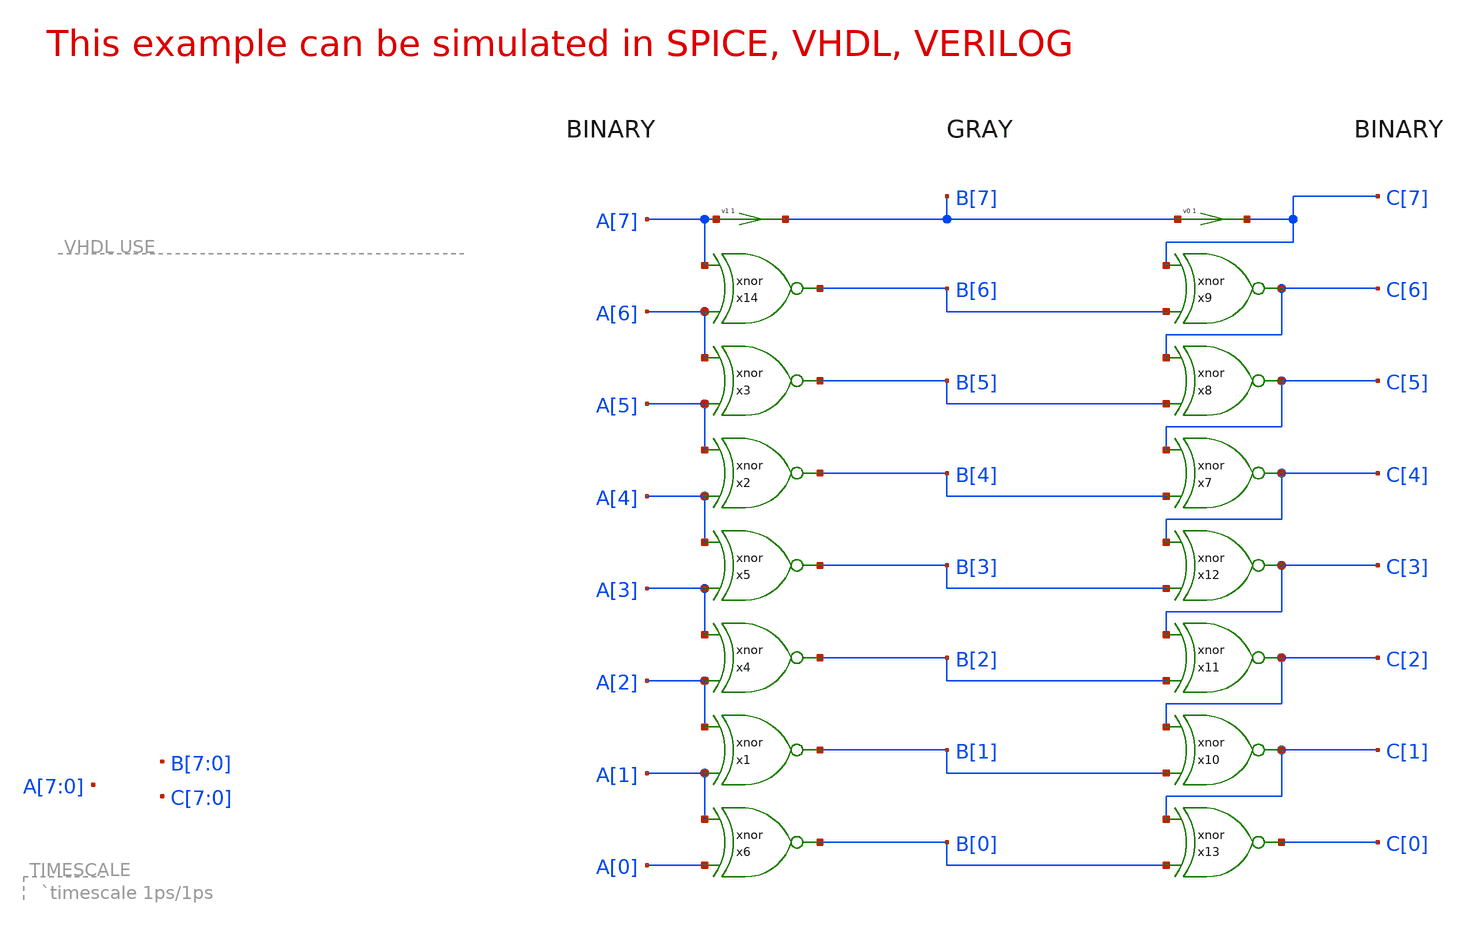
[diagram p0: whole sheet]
** sch_path: xschem_library/examples/greycnt.sch
**.subckt greycnt
v1 B[7] A[7] 0
v0 C[7] B[7] 0
**** begin user architecture code

.tran 1n 2000n

* to generate following file copy .../share/doc/xschem/examples/stimuli.greycnt
* to the simulation directory and run simulation -> Utile Stimuli Editor (GUI),
* and press 'Translate'
.include stimuli_greycnt.cir

.model nmos NMOS  LEVEL=1  LMIN=0.5e-6 LMAX=50e-6 WMIN=0.9e-6 WMAX=1  VTO=0.7 GAMMA=0.45 PHI=0.9
+  NSUB=9e14 LD=0.08e-6 UO=350 LAMBDA=0.1  TOX=9e-9 PB=0.9 CJ=0.56e-3 CJSW=0.35e-11  MJ=0.45 MJSW=0.2
+ CGDO=0.4e-9 JS=1.0e-8
.model pmos PMOS  LEVEL=1  LMIN=0.5e-6 LMAX=50e-6 WMIN=0.9e-6 WMAX=1  VTO=-0.8 GAMMA=0.4 PHI=0.8
+  NSUB=5e14 LD=0.09e-6 UO=100 LAMBDA=0.2  TOX=9e-9 PB=0.9 CJ=0.94e-3 CJSW=0.32e-11  MJ=0.5 MJSW=0.3 CGDO=0.3e-9
+ JS=0.5e-8
**** end user architecture code
**.ends
.end
